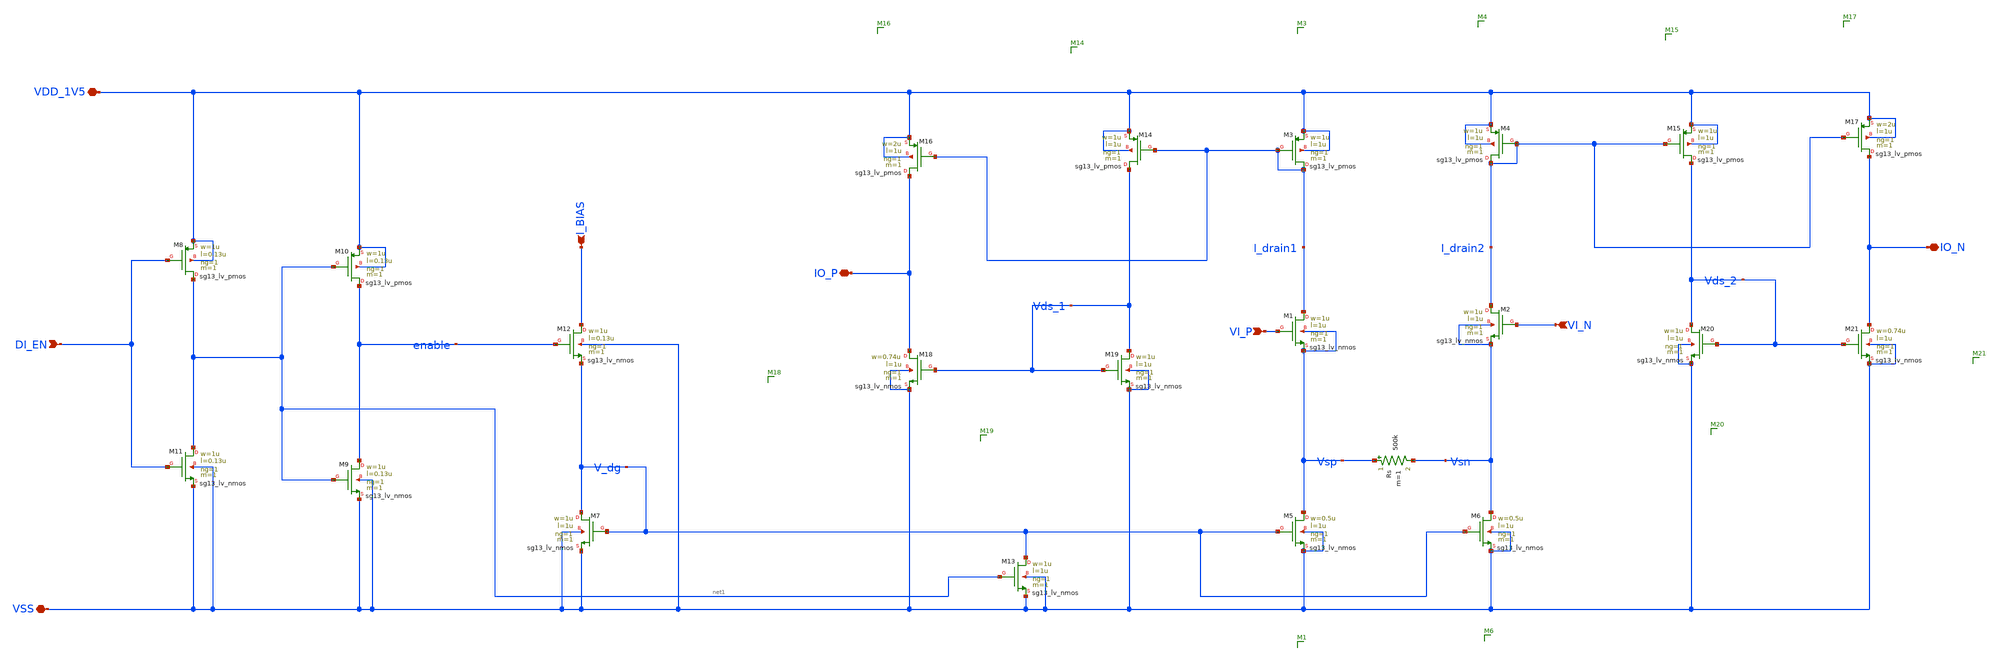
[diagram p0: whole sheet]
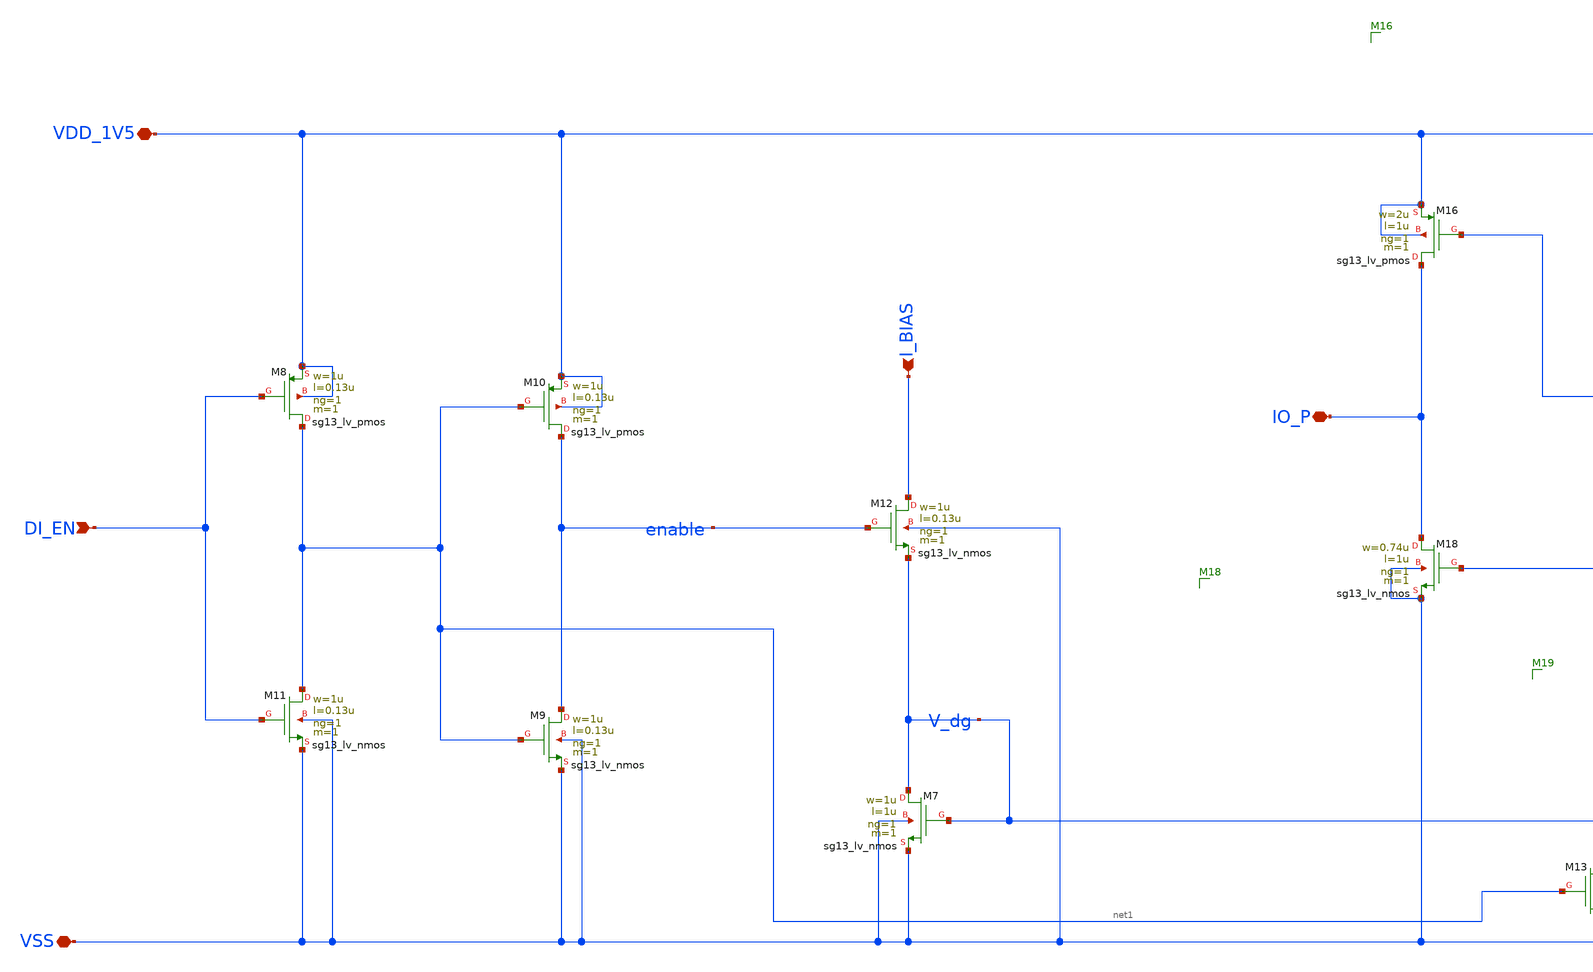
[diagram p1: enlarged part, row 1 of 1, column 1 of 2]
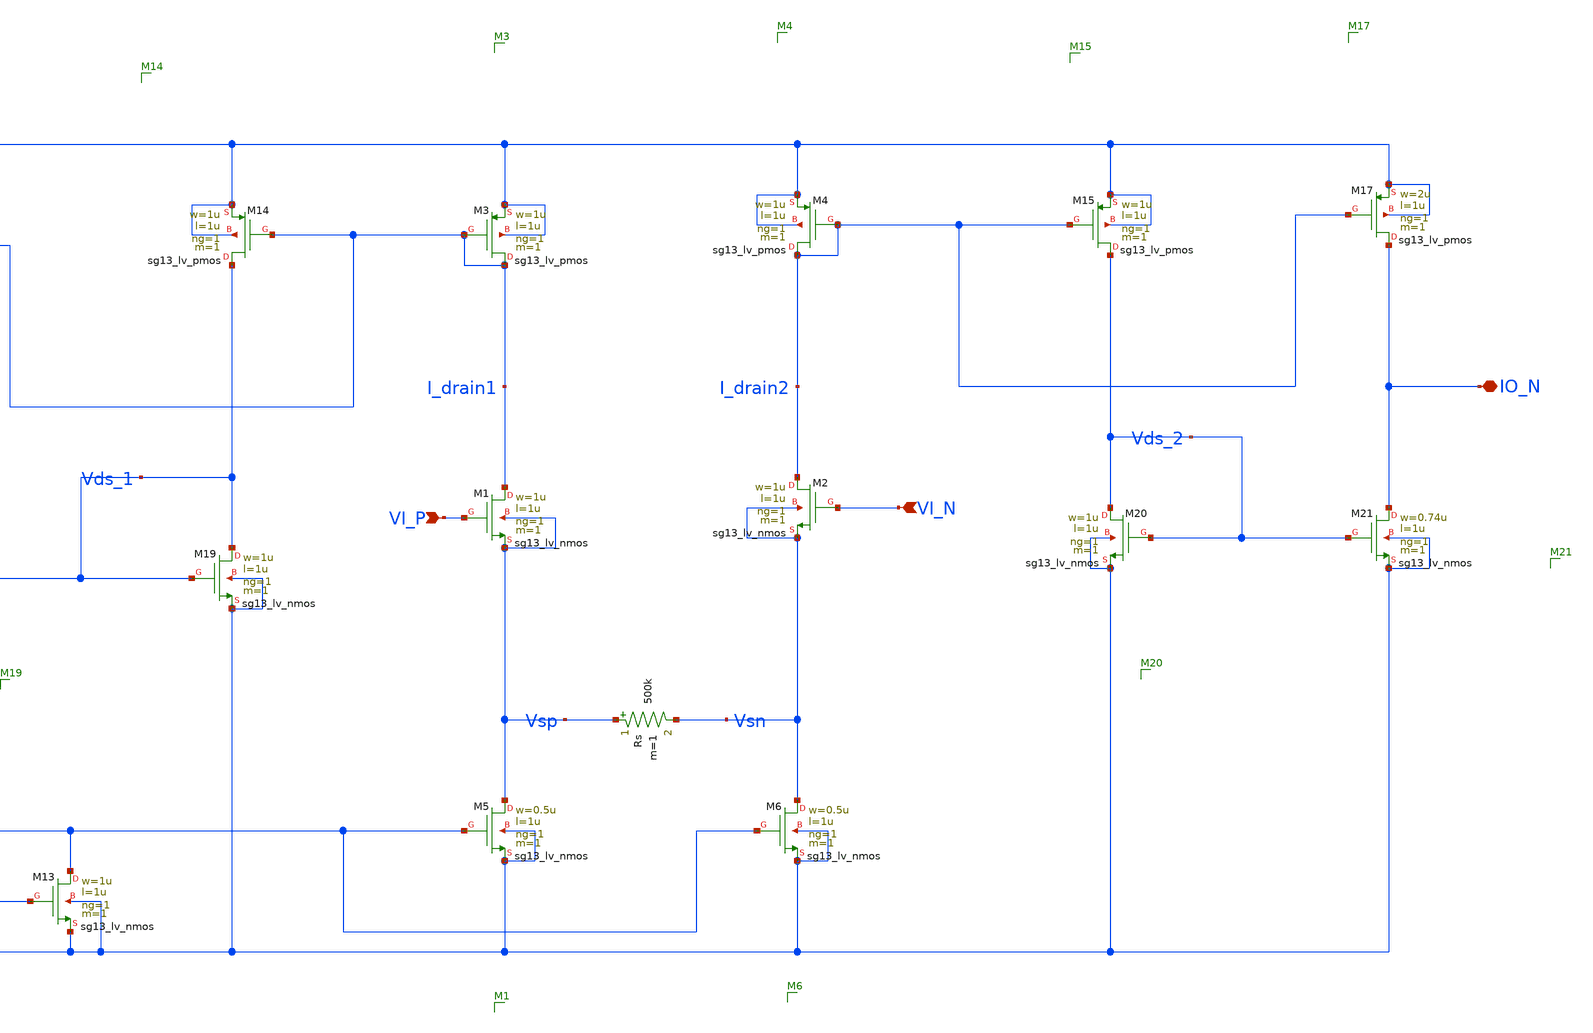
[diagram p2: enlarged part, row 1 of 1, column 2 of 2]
** sch_path: gm2.sch
**.subckt gm2 VI_N VI_P VSS VDD_1V5 IO_P IO_N I_BIAS DI_EN
*.ipin VI_N
*.ipin VI_P
*.iopin VSS
*.iopin VDD_1V5
*.iopin IO_P
*.iopin IO_N
*.ipin I_BIAS
*.ipin DI_EN
XM1 I_drain1 VI_P Vsp Vsp sg13_lv_nmos w=1u l=1u ng=1 m=1 mm_ok=1
XM2 I_drain2 VI_N Vsn Vsn sg13_lv_nmos w=1u l=1u ng=1 m=1 mm_ok=1
Rs Vsp Vsn 500k m=1
XM5 Vsp V_dg VSS VSS sg13_lv_nmos w=0.5u l=1u ng=1 m=1 mm_ok=1
XM6 Vsn V_dg VSS VSS sg13_lv_nmos w=0.5u l=1u ng=1 m=1 mm_ok=1
XM7 V_dg V_dg VSS VSS sg13_lv_nmos w=1u l=1u ng=1 m=1 mm_ok=1
XM8 net1 DI_EN VDD_1V5 VDD_1V5 sg13_lv_pmos w=1u l=0.13u ng=1 m=1 mm_ok=1
XM9 enable net1 VSS VSS sg13_lv_nmos w=1u l=0.13u ng=1 m=1 mm_ok=1
XM10 enable net1 VDD_1V5 VDD_1V5 sg13_lv_pmos w=1u l=0.13u ng=1 m=1 mm_ok=1
XM11 net1 DI_EN VSS VSS sg13_lv_nmos w=1u l=0.13u ng=1 m=1 mm_ok=1
XM12 I_BIAS enable V_dg VSS sg13_lv_nmos w=1u l=0.13u ng=1 m=1 mm_ok=1
XM3 I_drain1 I_drain1 VDD_1V5 VDD_1V5 sg13_lv_pmos w=1u l=1u ng=1 m=1 mm_ok=1
XM4 I_drain2 I_drain2 VDD_1V5 VDD_1V5 sg13_lv_pmos w=1u l=1u ng=1 m=1 mm_ok=1
XM14 Vds_1 I_drain1 VDD_1V5 VDD_1V5 sg13_lv_pmos w=1u l=1u ng=1 m=1 mm_ok=1
XM15 Vds_2 I_drain2 VDD_1V5 VDD_1V5 sg13_lv_pmos w=1u l=1u ng=1 m=1 mm_ok=1
XM13 V_dg net1 VSS VSS sg13_lv_nmos w=1u l=1u ng=1 m=1 mm_ok=1
XM16 IO_P I_drain1 VDD_1V5 VDD_1V5 sg13_lv_pmos w=2u l=1u ng=1 m=1 mm_ok=1
XM17 IO_N I_drain2 VDD_1V5 VDD_1V5 sg13_lv_pmos w=2u l=1u ng=1 m=1 mm_ok=1
XM18 IO_P Vds_1 VSS VSS sg13_lv_nmos w=0.74u l=1u ng=1 m=1 mm_ok=1
XM19 Vds_1 Vds_1 VSS VSS sg13_lv_nmos w=1u l=1u ng=1 m=1 mm_ok=1
XM20 Vds_2 Vds_2 VSS VSS sg13_lv_nmos w=1u l=1u ng=1 m=1 mm_ok=1
XM21 IO_N Vds_2 VSS VSS sg13_lv_nmos w=0.74u l=1u ng=1 m=1 mm_ok=1
**.ends
.end
